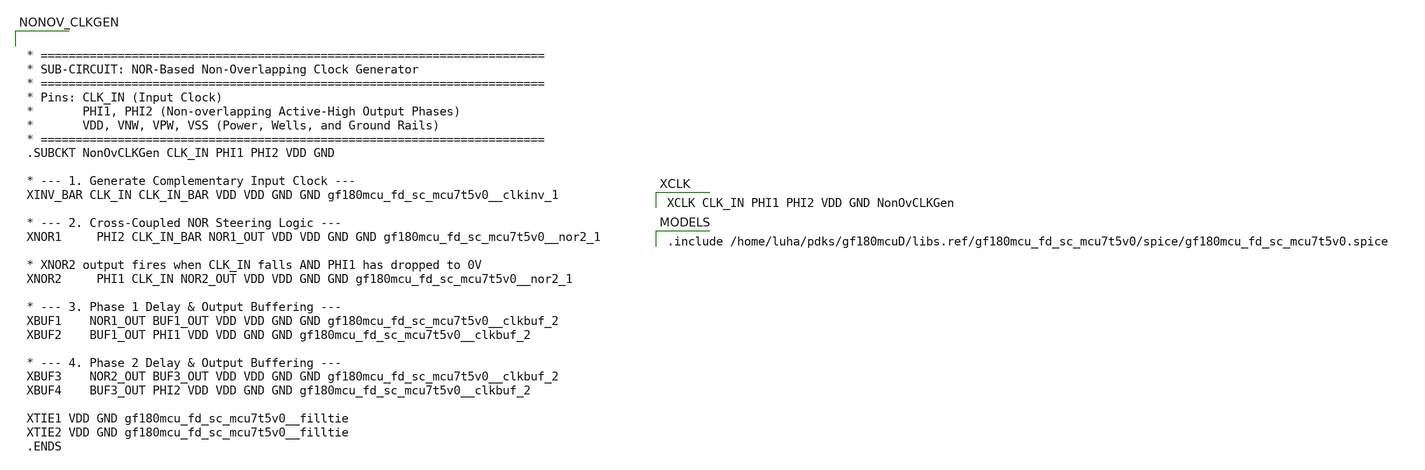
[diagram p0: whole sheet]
** sch_path: 1_Design/GF180_cells/NonOvCLKGen/design/NonOvCLKGen.sch
**.subckt NonOvCLKGen
**** begin user architecture code
 .include /home/luha/pdks/gf180mcuD/libs.ref/gf180mcu_fd_sc_mcu7t5v0/spice/gf180mcu_fd_sc_mcu7t5v0.spice


XCLK CLK_IN PHI1 PHI2 VDD GND NonOvCLKGen



* ========================================================================
* SUB-CIRCUIT: NOR-Based Non-Overlapping Clock Generator
* ========================================================================
* Pins: CLK_IN (Input Clock)
*       PHI1, PHI2 (Non-overlapping Active-High Output Phases)
*       VDD, VNW, VPW, VSS (Power, Wells, and Ground Rails)
* ========================================================================
.SUBCKT NonOvCLKGen CLK_IN PHI1 PHI2 VDD GND

* --- 1. Generate Complementary Input Clock ---
XINV_BAR CLK_IN CLK_IN_BAR VDD VDD GND GND gf180mcu_fd_sc_mcu7t5v0__clkinv_1

* --- 2. Cross-Coupled NOR Steering Logic ---
XNOR1	 PHI2 CLK_IN_BAR NOR1_OUT VDD VDD GND GND gf180mcu_fd_sc_mcu7t5v0__nor2_1

* XNOR2 output fires when CLK_IN falls AND PHI1 has dropped to 0V
XNOR2	 PHI1 CLK_IN NOR2_OUT VDD VDD GND GND gf180mcu_fd_sc_mcu7t5v0__nor2_1

* --- 3. Phase 1 Delay & Output Buffering ---
XBUF1    NOR1_OUT BUF1_OUT VDD VDD GND GND gf180mcu_fd_sc_mcu7t5v0__clkbuf_2
XBUF2    BUF1_OUT PHI1 VDD VDD GND GND gf180mcu_fd_sc_mcu7t5v0__clkbuf_2

* --- 4. Phase 2 Delay & Output Buffering ---
XBUF3    NOR2_OUT BUF3_OUT VDD VDD GND GND gf180mcu_fd_sc_mcu7t5v0__clkbuf_2
XBUF4    BUF3_OUT PHI2 VDD VDD GND GND gf180mcu_fd_sc_mcu7t5v0__clkbuf_2

XTIE1 VDD GND gf180mcu_fd_sc_mcu7t5v0__filltie
XTIE2 VDD GND gf180mcu_fd_sc_mcu7t5v0__filltie
.ENDS


**** end user architecture code
**.ends
.end
